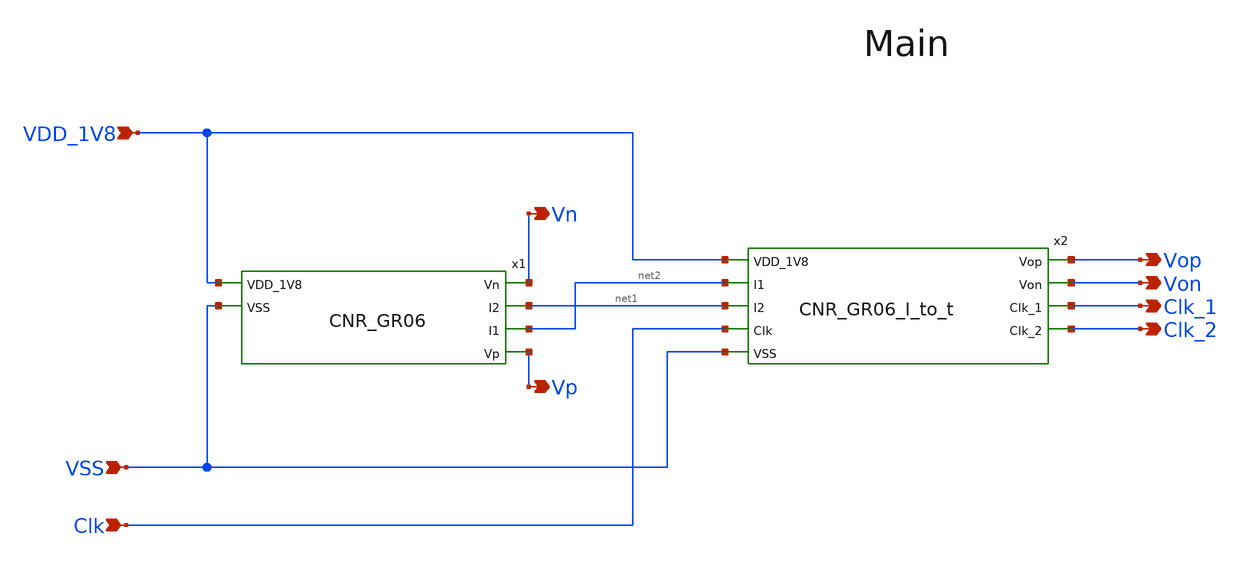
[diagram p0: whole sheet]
** sch_path: design/CNR_GR06_SKY130NM/CNR_GR06_main.sch
**.subckt CNR_GR06_main VDD_1V8 VSS Vn Vp Vop Von Clk_1 Clk_2 Clk
*.ipin VDD_1V8
*.ipin VSS
*.opin Vn
*.opin Vp
*.opin Vop
*.opin Von
*.opin Clk_1
*.opin Clk_2
*.ipin Clk
x1 VDD_1V8 Vn net1 net2 Vp VSS CNR_GR06
x2 VDD_1V8 net2 Vop Von net1 Clk_1 Clk Clk_2 VSS CNR_GR06_I_to_t
**.ends
.end
